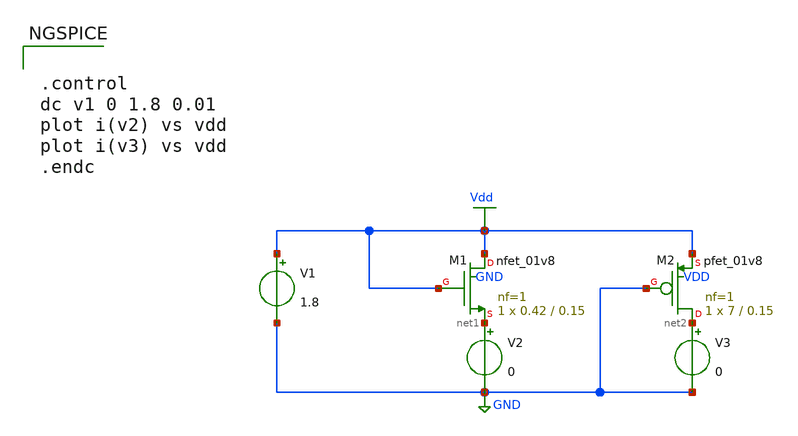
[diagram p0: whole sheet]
** sch_path: Circuiti/confronto corrente.sch
**.subckt confronto corrente
XM1 Vdd Vdd net1 GND sky130_fd_pr__nfet_01v8 L=0.15 W=0.42 nf=1 ad='int((nf+1)/2) * W/nf * 0.29' as='int((nf+2)/2) * W/nf * 0.29'
+ pd='2*int((nf+1)/2) * (W/nf + 0.29)' ps='2*int((nf+2)/2) * (W/nf + 0.29)' nrd='0.29 / W' nrs='0.29 / W'
+ sa=0 sb=0 sd=0 mult=1 m=1
V1 Vdd GND 1.8
V2 net1 GND 0
XM2 net2 GND Vdd VDD sky130_fd_pr__pfet_01v8 L=0.15 W=7 nf=1 ad='int((nf+1)/2) * W/nf * 0.29' as='int((nf+2)/2) * W/nf * 0.29'
+ pd='2*int((nf+1)/2) * (W/nf + 0.29)' ps='2*int((nf+2)/2) * (W/nf + 0.29)' nrd='0.29 / W' nrs='0.29 / W'
+ sa=0 sb=0 sd=0 mult=1 m=1
V3 net2 GND 0
**** begin user architecture code


.lib /home/matteo/xschem_downloads/skywater-pdk/libraries/sky130_fd_pr_ngspice/latest/models/sky130.lib.spice tt

*.include /home/matteo/xschem_downloads/skywater-pdk/libraries/sky130_fd_pr_ngspice/latest/cells/nfet_01v8/sky130_fd_pr__nfet_01v8__tt.corner.spice

.param mc_mm_switch=0
.param mc_pr_switch=1




.control
dc v1 0 1.8 0.01
plot i(v2) vs vdd
plot i(v3) vs vdd
.endc


**** end user architecture code
**.ends
.GLOBAL GND
.GLOBAL Vdd
.end
